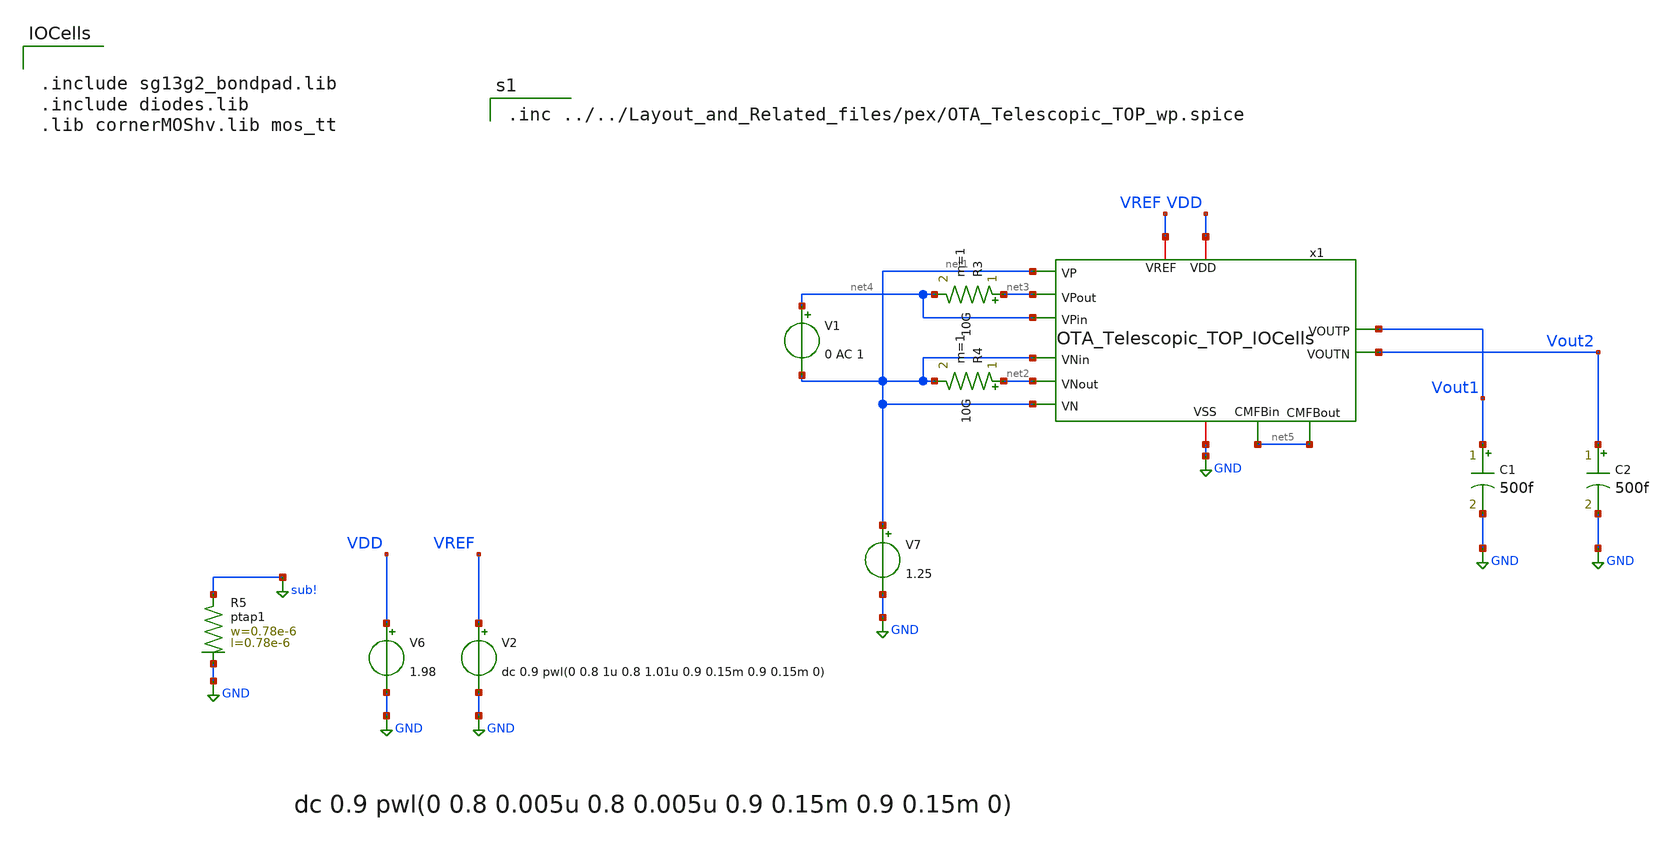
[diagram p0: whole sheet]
** sch_path: OTA_Telescopic/Testbenchs/OTA_Telescopic_TOP_TB_OL_io.sch
**.subckt OTA_Telescopic_TOP_TB_OL_io
V7 net1 GND 1.25
C1 Vout1 GND 500f m=1
C2 Vout2 GND 500f m=1
V6 VDD GND 1.98
R3 net3 net4 10G m=1
R4 net2 net1 10G m=1
V1 net4 net1 0 AC 1
V2 VREF GND dc 0.9 pwl(0 0.8 1u 0.8 1.01u 0.9 0.15m 0.9 0.15m 0)
XR5 sub! GND ptap1 R=262.8 w=0.78e-6 l=0.78e-6
x1 VDD GND net3 net1 net4 Vout2 Vout1 net1 net2 net1 VREF net5 net5 OTA_Telescopic_TOP_IOCells
**** begin user architecture code

** opencircuitdesign pdks install
.lib cornerMOSlv.lib mos_ff
.lib cornerRES.lib res_typ
.lib cornerCAP.lib cap_typ
.temp 0



.control
*save all
 set color0 = white

* AC simulation
ac dec 1k 1 1T
let Av = db((v(Vout2)-v(Vout1)))
meas ac Ao FIND Av WHEN frequency=10
let ABW = Ao-3
meas ac BW WHEN Av=ABW
meas ac UGBW WHEN Av=0
let phase_vec = 180/pi*cph(v(Vout2)-v(Vout1))

* Phase margin (PM)
meas ac phase FIND phase_vec WHEN frequency=UGBW
let PM = phase+180
print PM

* Gain margin (GM)
meas ac freq180 FIND frequency WHEN phase_vec=-180
meas ac gain FIND Av WHEN frequency=freq180
let GM = 0-gain

*BW in 7 dB
meas ac UGBW7dB WHEN Av=7
meas ac UGBW4dB WHEN Av=4

print GM
plot Av
plot phase_vec

plot db(v(x1.Vo1)-v(x1.Vo2))

write AC_OL.raw

wrdata AvOL_ Av
wrdata PhaseOL_ phase_vec


*DC simulation

op
let vout_dc = v(Vout1)
print vout_dc
write OTA_Telescopic_TOP_TB_OL.raw


reset
*noise v(Vout1) V6 dec 100 1 0.5e9 1
setplot noise1
*plot onoise_spectrum
setplot noise2
print onoise_total

.endc




.include sg13g2_bondpad.lib
.include diodes.lib
.lib cornerMOShv.lib mos_tt



.inc ../../Layout_and_Related_files/pex/OTA_Telescopic_TOP_wp.spice

**** end user architecture code
**.ends
.GLOBAL GND
.GLOBAL sub!
.end
